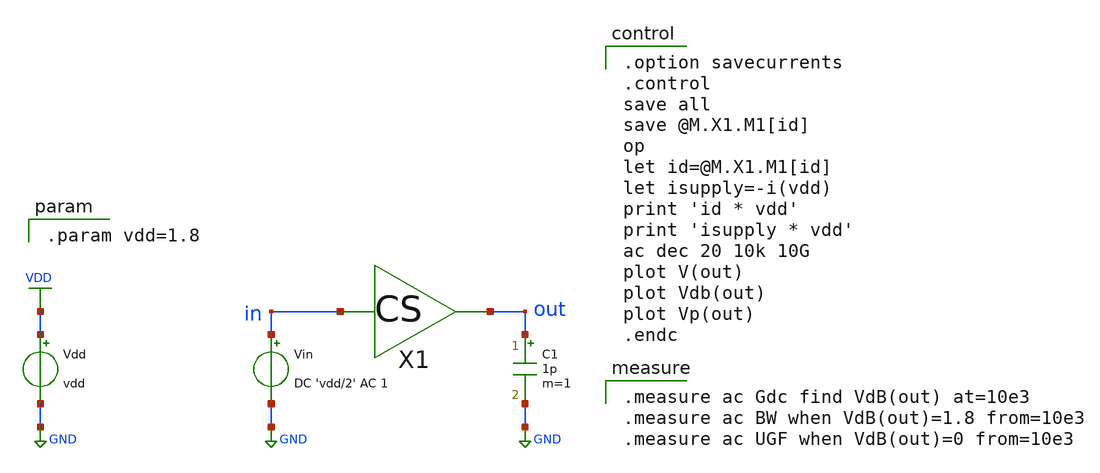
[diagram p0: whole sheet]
** sch_path: xschem/tb/ac_01.sch
**.subckt ac_01
Vdd VDD GND vdd
Vin in GND DC 'vdd/2' AC 1
X1 in out cs
C1 out GND 1p m=1
**** begin user architecture code

.model nch nmos ( version=4.7 level=54 lmin=0.1u lmax=20u wmin=0.1u wmax=10u  )
.model pch pmos ( version=4.7 level=54 lmin=0.1u lmax=20u wmin=0.1u wmax=10u  )


.option savecurrents
.control
save all
save @M.X1.M1[id]
op
let id=@M.X1.M1[id]
let isupply=-i(vdd)
print 'id * vdd'
print 'isupply * vdd'
ac dec 20 10k 10G
plot V(out)
plot Vdb(out)
plot Vp(out)
.endc


.measure ac Gdc find VdB(out) at=10e3
.measure ac BW when VdB(out)=1.8 from=10e3
.measure ac UGF when VdB(out)=0 from=10e3


.param vdd=1.8

**** end user architecture code
**.ends

* expanding   symbol:  /home/tsuchiya/tmp/openmpw-transistor-level-examples/xschem/tb/cs.sym # of
*+ pins=2
** sym_path: xschem/tb/cs.sym
** sch_path: xschem/tb/cs.sch
.subckt cs in out
*.ipin in
*.opin out
R1 VDD out 1k m=1
M1 out in GND GND nch w=3.6u l=0.18u m=1
.ends

.GLOBAL VDD
.GLOBAL GND
.end
